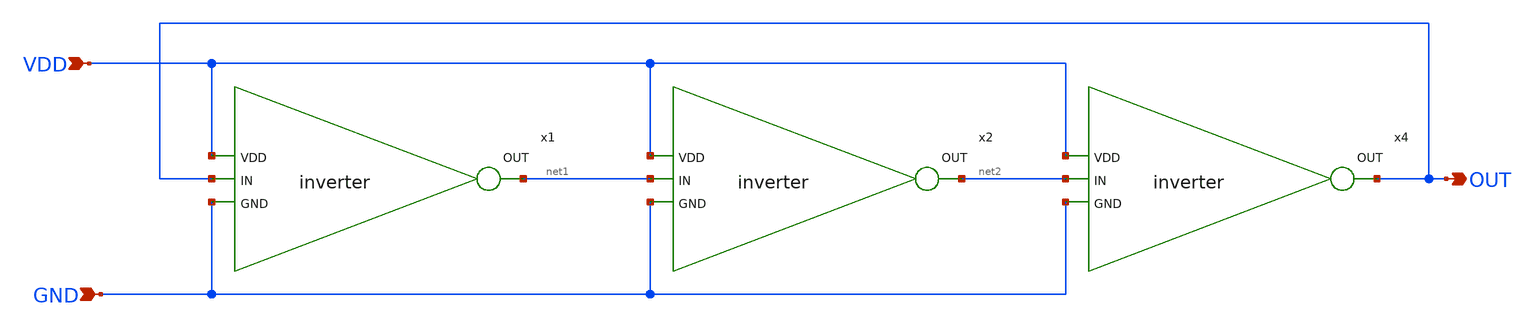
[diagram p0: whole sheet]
** sch_path: Inverter_RingOsc/ring_osilator.sch
**.subckt ring_osilator VDD OUT GND
*.ipin VDD
*.opin OUT
*.ipin GND
x4 VDD net2 OUT GND inverter
x1 VDD OUT net1 GND inverter
x2 VDD net1 net2 GND inverter
**.ends

* expanding   symbol:  inverter.sym # of pins=4
** sym_path: Inverter_RingOsc/inverter.sym
** sch_path: Inverter_RingOsc/inverter.sch
.subckt inverter VDD IN OUT GND
*.ipin GND
*.ipin IN
*.ipin VDD
*.opin OUT
XM1 OUT IN GND GND sky130_fd_pr__nfet_01v8 L=0.15 W=1 nf=1 ad='int((nf+1)/2) * W/nf * 0.29' as='int((nf+2)/2) * W/nf * 0.29'
+ pd='2*int((nf+1)/2) * (W/nf + 0.29)' ps='2*int((nf+2)/2) * (W/nf + 0.29)' nrd='0.29 / W' nrs='0.29 / W'
+ sa=0 sb=0 sd=0 mult=1 m=1
XM2 OUT IN VDD VDD sky130_fd_pr__pfet_01v8 L=0.15 W=1 nf=1 ad='int((nf+1)/2) * W/nf * 0.29' as='int((nf+2)/2) * W/nf * 0.29'
+ pd='2*int((nf+1)/2) * (W/nf + 0.29)' ps='2*int((nf+2)/2) * (W/nf + 0.29)' nrd='0.29 / W' nrs='0.29 / W'
+ sa=0 sb=0 sd=0 mult=1 m=1
.ends

.end
